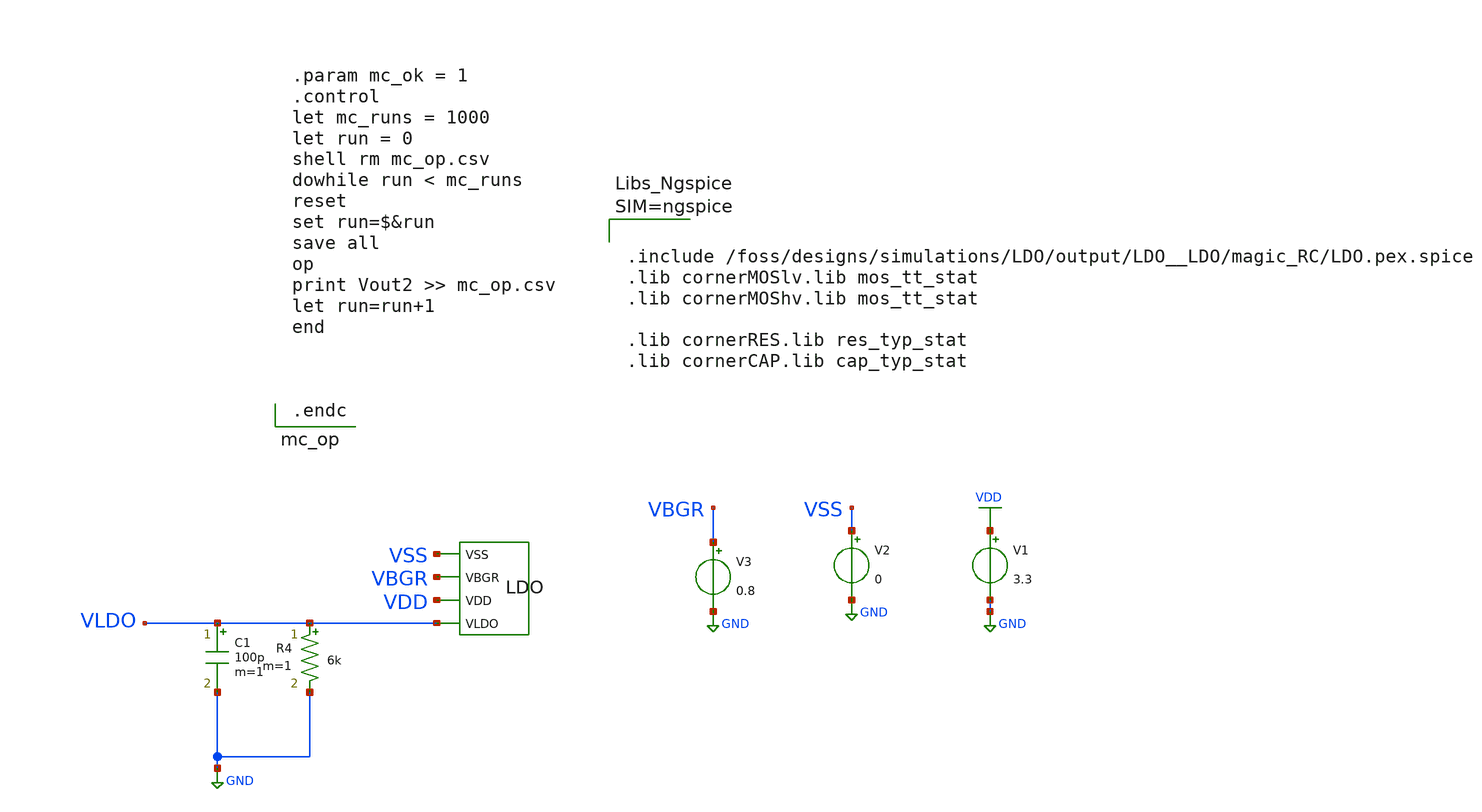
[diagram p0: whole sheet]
** sch_path: dependencies/LDO/LDO-main/testbenches/corners/xschem/ldo_post_layout_sim_mc.sch
**.subckt ldo_post_layout_sim_mc
V3 VBGR GND 0.8
V2 VSS GND 0
X1 VSS VBGR VDD VLDO LDO
C1 VLDO GND 100p m=1
R4 VLDO GND 6k m=1
V1 VDD GND 3.3
**** begin user architecture code



.include /foss/designs/simulations/LDO/output/LDO__LDO/magic_RC/LDO.pex.spice
.lib cornerMOSlv.lib mos_tt_stat
.lib cornerMOShv.lib mos_tt_stat

.lib cornerRES.lib res_typ_stat
.lib cornerCAP.lib cap_typ_stat






.param mc_ok = 1
.control
let mc_runs = 1000
let run = 0
shell rm mc_op.csv
dowhile run < mc_runs
reset
set run=$&run
save all
op
print Vout2 >> mc_op.csv
let run=run+1
end



.endc

**** end user architecture code
**.ends
.GLOBAL GND
.GLOBAL VDD
.end
